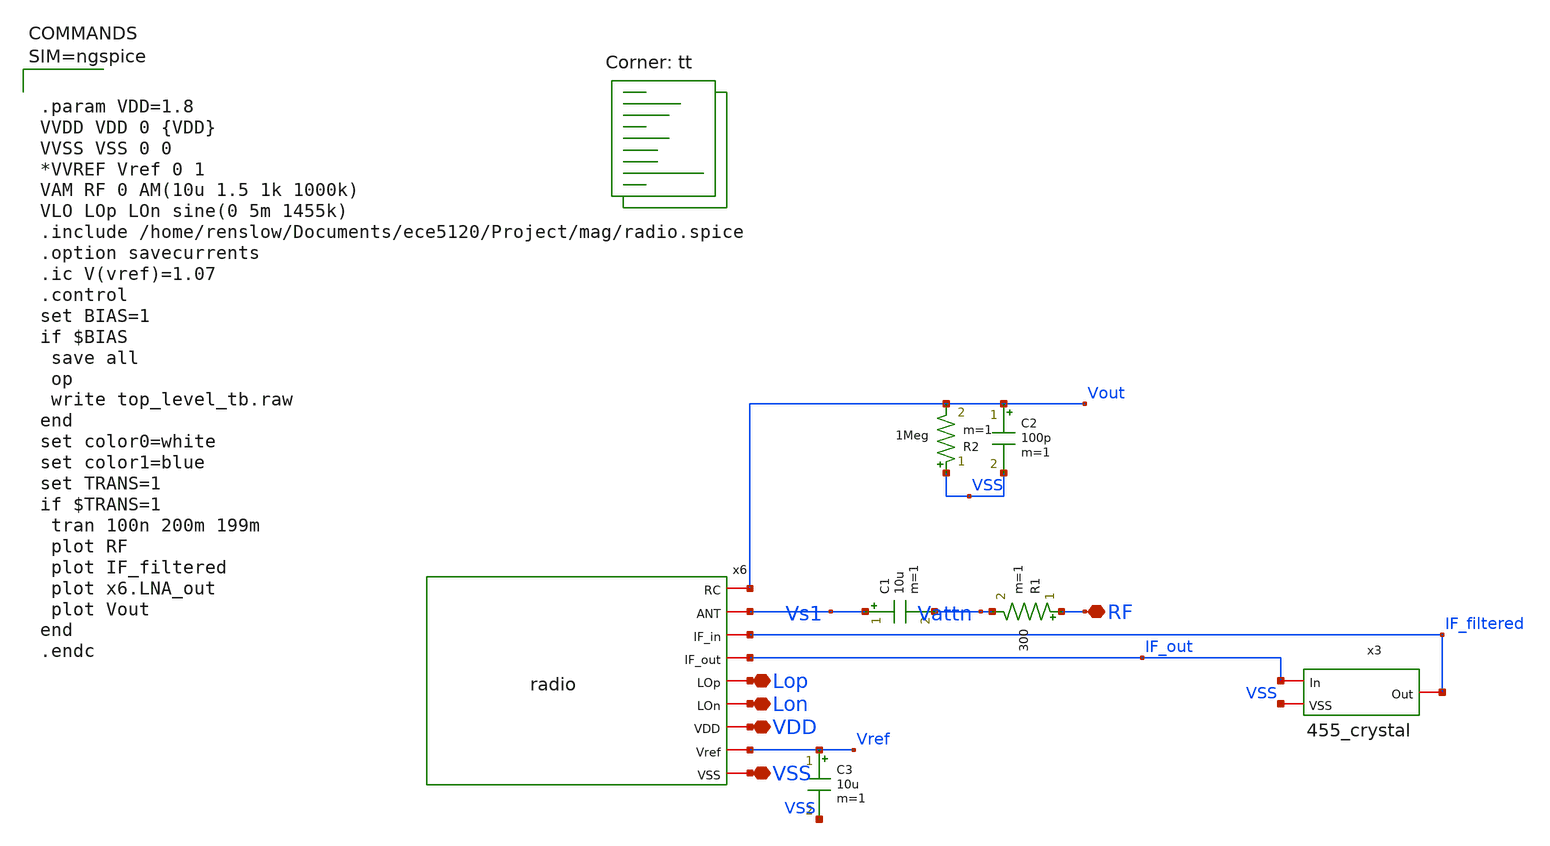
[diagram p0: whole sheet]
** sch_path: Project/mag/top _level_tb.sch
**.subckt top _level_tb VDD RF VSS Lop Lon
*.iopin VDD
*.iopin RF
*.iopin VSS
*.iopin Lop
*.iopin Lon
C1 Vs1 Vattn 10u m=1
R1 RF Vattn 300 m=1
x3 IF_out IF_filtered VSS 455_crystal
R2 VSS Vout 1Meg m=1
C2 Vout VSS 100p m=1
C3 Vref VSS 10u m=1
x6 Vout Vs1 IF_filtered IF_out Lop Lon VDD Vref VSS radio
**** begin user architecture code



.param VDD=1.8
VVDD VDD 0 {VDD}
VVSS VSS 0 0
*VVREF Vref 0 1
VAM RF 0 AM(10u 1.5 1k 1000k)
VLO LOp LOn sine(0 5m 1455k)
.include /home/renslow/Documents/ece5120/Project/mag/radio.spice
.option savecurrents
.ic V(vref)=1.07
.control
set BIAS=1
if $BIAS
 save all
 op
 write top_level_tb.raw
end
set color0=white
set color1=blue
set TRANS=1
if $TRANS=1
 tran 100n 200m 199m
 plot RF
 plot IF_filtered
 plot x6.LNA_out
 plot Vout
end
.endc



.lib $::SKYWATER_MODELS/sky130.lib.spice tt
**** end user architecture code
**.ends
.end
